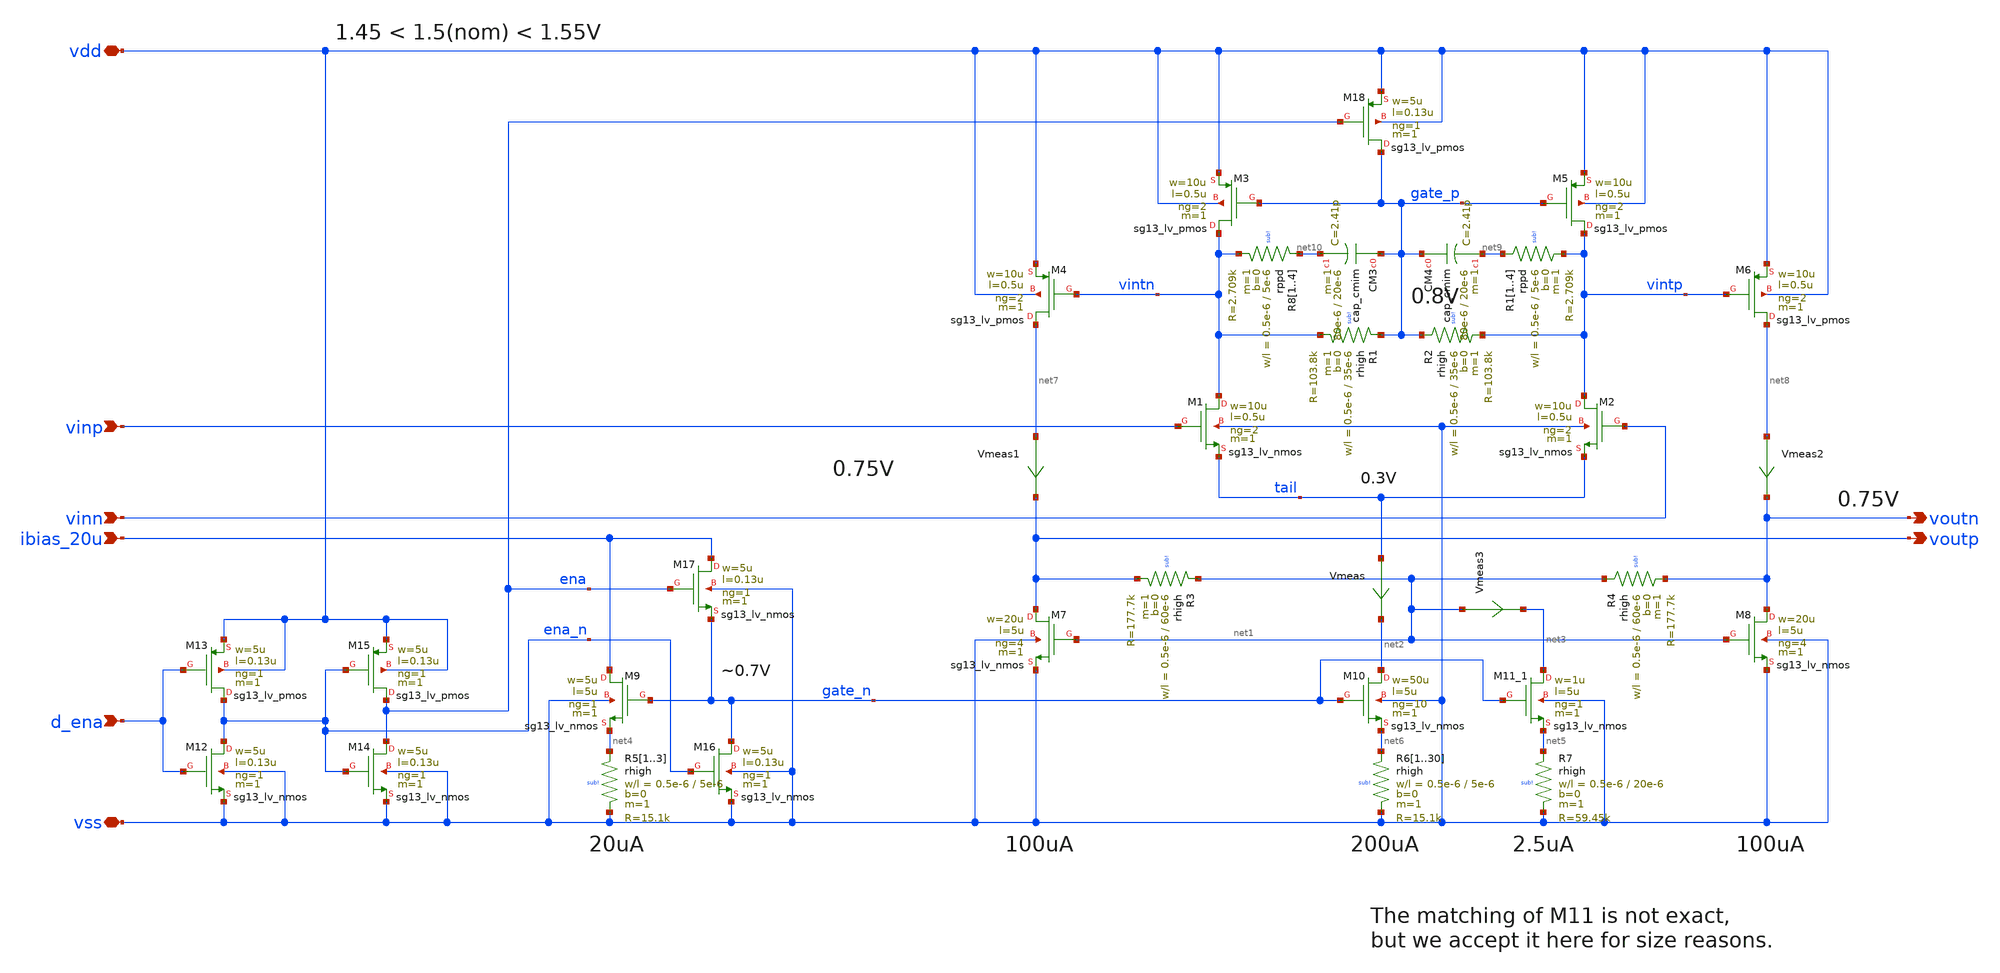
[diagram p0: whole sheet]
** sch_path: xschem/ota-diff.sch
* (c) 2025 H. Pretl, Apache-2.0 license
**.subckt ota-diff ibias_20u vdd vss vinp vinn voutp d_ena voutn
*.ipin ibias_20u
*.iopin vdd
*.iopin vss
*.ipin vinp
*.ipin vinn
*.opin voutp
*.ipin d_ena
*.opin voutn
XM10 net2 gate_n net6 vss sg13_lv_nmos w=50u l=5u ng=10 m=1 mm_ok=1
XM1 vintn vinp tail vss sg13_lv_nmos w=10u l=0.5u ng=2 m=1 mm_ok=1
XM2 vintp vinn tail vss sg13_lv_nmos w=10u l=0.5u ng=2 m=1 mm_ok=1
XM3 vintn gate_p vdd vdd sg13_lv_pmos w=10u l=0.5u ng=2 m=1 mm_ok=1
XM9 ibias_20u gate_n net4 vss sg13_lv_nmos w=5u l=5u ng=1 m=1 mm_ok=1
XM16 gate_n ena_n vss vss sg13_lv_nmos w=5u l=0.13u ng=1 m=1 mm_ok=1
XM18 gate_p ena vdd vdd sg13_lv_pmos w=5u l=0.13u ng=1 m=1 mm_ok=1
XM14 ena ena_n vss vss sg13_lv_nmos w=5u l=0.13u ng=1 m=1 mm_ok=1
XM15 ena ena_n vdd vdd sg13_lv_pmos w=5u l=0.13u ng=1 m=1 mm_ok=1
XM17 ibias_20u ena gate_n vss sg13_lv_nmos w=5u l=0.13u ng=1 m=1 mm_ok=1
XM12 ena_n d_ena vss vss sg13_lv_nmos w=5u l=0.13u ng=1 m=1 mm_ok=1
XM13 ena_n d_ena vdd vdd sg13_lv_pmos w=5u l=0.13u ng=1 m=1 mm_ok=1
XM7 voutp net1 vss vss sg13_lv_nmos w=20u l=5u ng=4 m=1 mm_ok=1
XR1 gate_p vintn sub! rhigh w=0.5e-6 l=35e-6 m=1 b=0 mm_ok=1
XR3 net1 voutp sub! rhigh w=0.5e-6 l=60e-6 m=1 b=0 mm_ok=1
XM11_1 net3 gate_n net5 vss sg13_lv_nmos w=1u l=5u ng=1 m=1 mm_ok=1
XM5 vintp gate_p vdd vdd sg13_lv_pmos w=10u l=0.5u ng=2 m=1 mm_ok=1
XM4 net7 vintn vdd vdd sg13_lv_pmos w=10u l=0.5u ng=2 m=1 mm_ok=1
XM6 net8 vintp vdd vdd sg13_lv_pmos w=10u l=0.5u ng=2 m=1 mm_ok=1
XR2 gate_p vintp sub! rhigh w=0.5e-6 l=35e-6 m=1 b=0 mm_ok=1
XM8 voutn net1 vss vss sg13_lv_nmos w=20u l=5u ng=4 m=1 mm_ok=1
XR4 net1 voutn sub! rhigh w=0.5e-6 l=60e-6 m=1 b=0 mm_ok=1
Vmeas tail net2 0
.save i(vmeas)
Vmeas1 net7 voutp 0
.save i(vmeas1)
Vmeas2 net8 voutn 0
.save i(vmeas2)
Vmeas3 net1 net3 0
.save i(vmeas3)
XR51 net4 vss sub! rhigh w=0.5e-6 l=5e-6 m=1 b=0 mm_ok=1
XR52 net4 vss sub! rhigh w=0.5e-6 l=5e-6 m=1 b=0 mm_ok=1
XR53 net4 vss sub! rhigh w=0.5e-6 l=5e-6 m=1 b=0 mm_ok=1
XR7 net5 vss sub! rhigh w=0.5e-6 l=20e-6 m=1 b=0 mm_ok=1
XR61 net6 vss sub! rhigh w=0.5e-6 l=5e-6 m=1 b=0 mm_ok=1
XR62 net6 vss sub! rhigh w=0.5e-6 l=5e-6 m=1 b=0 mm_ok=1
XR63 net6 vss sub! rhigh w=0.5e-6 l=5e-6 m=1 b=0 mm_ok=1
XR64 net6 vss sub! rhigh w=0.5e-6 l=5e-6 m=1 b=0 mm_ok=1
XR65 net6 vss sub! rhigh w=0.5e-6 l=5e-6 m=1 b=0 mm_ok=1
XR66 net6 vss sub! rhigh w=0.5e-6 l=5e-6 m=1 b=0 mm_ok=1
XR67 net6 vss sub! rhigh w=0.5e-6 l=5e-6 m=1 b=0 mm_ok=1
XR68 net6 vss sub! rhigh w=0.5e-6 l=5e-6 m=1 b=0 mm_ok=1
XR69 net6 vss sub! rhigh w=0.5e-6 l=5e-6 m=1 b=0 mm_ok=1
XR610 net6 vss sub! rhigh w=0.5e-6 l=5e-6 m=1 b=0 mm_ok=1
XR611 net6 vss sub! rhigh w=0.5e-6 l=5e-6 m=1 b=0 mm_ok=1
XR612 net6 vss sub! rhigh w=0.5e-6 l=5e-6 m=1 b=0 mm_ok=1
XR613 net6 vss sub! rhigh w=0.5e-6 l=5e-6 m=1 b=0 mm_ok=1
XR614 net6 vss sub! rhigh w=0.5e-6 l=5e-6 m=1 b=0 mm_ok=1
XR615 net6 vss sub! rhigh w=0.5e-6 l=5e-6 m=1 b=0 mm_ok=1
XR616 net6 vss sub! rhigh w=0.5e-6 l=5e-6 m=1 b=0 mm_ok=1
XR617 net6 vss sub! rhigh w=0.5e-6 l=5e-6 m=1 b=0 mm_ok=1
XR618 net6 vss sub! rhigh w=0.5e-6 l=5e-6 m=1 b=0 mm_ok=1
XR619 net6 vss sub! rhigh w=0.5e-6 l=5e-6 m=1 b=0 mm_ok=1
XR620 net6 vss sub! rhigh w=0.5e-6 l=5e-6 m=1 b=0 mm_ok=1
XR621 net6 vss sub! rhigh w=0.5e-6 l=5e-6 m=1 b=0 mm_ok=1
XR622 net6 vss sub! rhigh w=0.5e-6 l=5e-6 m=1 b=0 mm_ok=1
XR623 net6 vss sub! rhigh w=0.5e-6 l=5e-6 m=1 b=0 mm_ok=1
XR624 net6 vss sub! rhigh w=0.5e-6 l=5e-6 m=1 b=0 mm_ok=1
XR625 net6 vss sub! rhigh w=0.5e-6 l=5e-6 m=1 b=0 mm_ok=1
XR626 net6 vss sub! rhigh w=0.5e-6 l=5e-6 m=1 b=0 mm_ok=1
XR627 net6 vss sub! rhigh w=0.5e-6 l=5e-6 m=1 b=0 mm_ok=1
XR628 net6 vss sub! rhigh w=0.5e-6 l=5e-6 m=1 b=0 mm_ok=1
XR629 net6 vss sub! rhigh w=0.5e-6 l=5e-6 m=1 b=0 mm_ok=1
XR630 net6 vss sub! rhigh w=0.5e-6 l=5e-6 m=1 b=0 mm_ok=1
XCM3 gate_p net10 cap_cmim w=80e-6 l=20e-6 m=1 mm_ok=1
XCM4 gate_p net9 cap_cmim w=80e-6 l=20e-6 m=1 mm_ok=1
XR81 net10 vintn sub! rppd w=0.5e-6 l=5e-6 m=1 b=0 mm_ok=1
XR82 net10 vintn sub! rppd w=0.5e-6 l=5e-6 m=1 b=0 mm_ok=1
XR83 net10 vintn sub! rppd w=0.5e-6 l=5e-6 m=1 b=0 mm_ok=1
XR84 net10 vintn sub! rppd w=0.5e-6 l=5e-6 m=1 b=0 mm_ok=1
XR11 net9 vintp sub! rppd w=0.5e-6 l=5e-6 m=1 b=0 mm_ok=1
XR12 net9 vintp sub! rppd w=0.5e-6 l=5e-6 m=1 b=0 mm_ok=1
XR13 net9 vintp sub! rppd w=0.5e-6 l=5e-6 m=1 b=0 mm_ok=1
XR14 net9 vintp sub! rppd w=0.5e-6 l=5e-6 m=1 b=0 mm_ok=1
**.ends
.end
